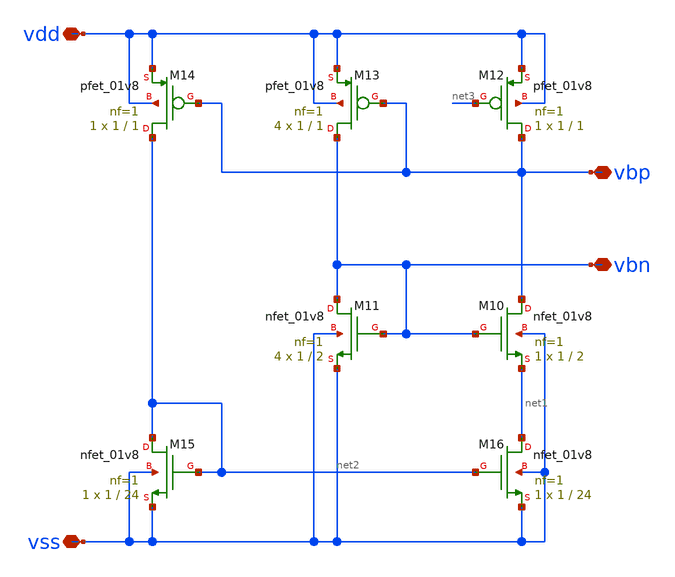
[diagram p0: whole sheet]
** sch_path: circuits/OgueyAebischerBias.sch
**.subckt OgueyAebischerBias vss vdd vbp vbn
*.iopin vss
*.iopin vdd
*.iopin vbp
*.iopin vbn
XM10 vbp vbn net1 vss sky130_fd_pr__nfet_01v8 L=2 W=1 nf=1 ad='int((1 + 1)/2) * 1 / 1 * 0.29' as='int((1 + 2)/2) * 1 / 1 * 0.29'
+ pd='2*int((1 + 1)/2) * (1 / 1 + 0.29)' ps='2*int((1 + 2)/2) * (1 / 1 + 0.29)' nrd='0.29 / 1 ' nrs='0.29 / 1 '
+ sa=0 sb=0 sd=0 mult=1 m=1
XM12 vbp net3 vdd vdd sky130_fd_pr__pfet_01v8 L=1 W=1 nf=1 ad='int((nf+1)/2) * W/nf * 0.29' as='int((nf+2)/2) * W/nf * 0.29'
+ pd='2*int((nf+1)/2) * (W/nf + 0.29)' ps='2*int((nf+2)/2) * (W/nf + 0.29)' nrd='0.29 / W' nrs='0.29 / W'
+ sa=0 sb=0 sd=0 mult=1 m=1
XM11 vbn vbn vss vss sky130_fd_pr__nfet_01v8 L=2 W=1 nf=1 ad='int((1 + 1)/2) * 1 / 1 * 0.29' as='int((1 + 2)/2) * 1 / 1 * 0.29'
+ pd='2*int((1 + 1)/2) * (1 / 1 + 0.29)' ps='2*int((1 + 2)/2) * (1 / 1 + 0.29)' nrd='0.29 / 1 ' nrs='0.29 / 1 '
+ sa=0 sb=0 sd=0 mult=4 m=4
XM13 vbn vbp vdd vdd sky130_fd_pr__pfet_01v8 L=1 W=1 nf=1 ad='int((nf+1)/2) * W/nf * 0.29' as='int((nf+2)/2) * W/nf * 0.29'
+ pd='2*int((nf+1)/2) * (W/nf + 0.29)' ps='2*int((nf+2)/2) * (W/nf + 0.29)' nrd='0.29 / W' nrs='0.29 / W'
+ sa=0 sb=0 sd=0 mult=4 m=4
XM14 net2 vbp vdd vdd sky130_fd_pr__pfet_01v8 L=1 W=1 nf=1 ad='int((nf+1)/2) * W/nf * 0.29' as='int((nf+2)/2) * W/nf * 0.29'
+ pd='2*int((nf+1)/2) * (W/nf + 0.29)' ps='2*int((nf+2)/2) * (W/nf + 0.29)' nrd='0.29 / W' nrs='0.29 / W'
+ sa=0 sb=0 sd=0 mult=1 m=1
XM16 net1 net2 vss vss sky130_fd_pr__nfet_01v8 L=24 W=1 nf=1 ad='int((1 + 1)/2) * 1 / 1 * 0.29' as='int((1 + 2)/2) * 1 / 1 * 0.29'
+ pd='2*int((1 + 1)/2) * (1 / 1 + 0.29)' ps='2*int((1 + 2)/2) * (1 / 1 + 0.29)' nrd='0.29 / 1 ' nrs='0.29 / 1 '
+ sa=0 sb=0 sd=0 mult=1 m=1
XM15 net2 net2 vss vss sky130_fd_pr__nfet_01v8 L=24 W=1 nf=1 ad='int((1 + 1)/2) * 1 / 1 * 0.29' as='int((1 + 2)/2) * 1 / 1 * 0.29'
+ pd='2*int((1 + 1)/2) * (1 / 1 + 0.29)' ps='2*int((1 + 2)/2) * (1 / 1 + 0.29)' nrd='0.29 / 1 ' nrs='0.29 / 1 '
+ sa=0 sb=0 sd=0 mult=1 m=1
**** begin user architecture code
 .lib $::SKYWATER_MODELS/models/sky130.lib.spice tt

.param mc_mm_switch=0
.param mc_pr_switch=1


**** end user architecture code
**.ends
.end
